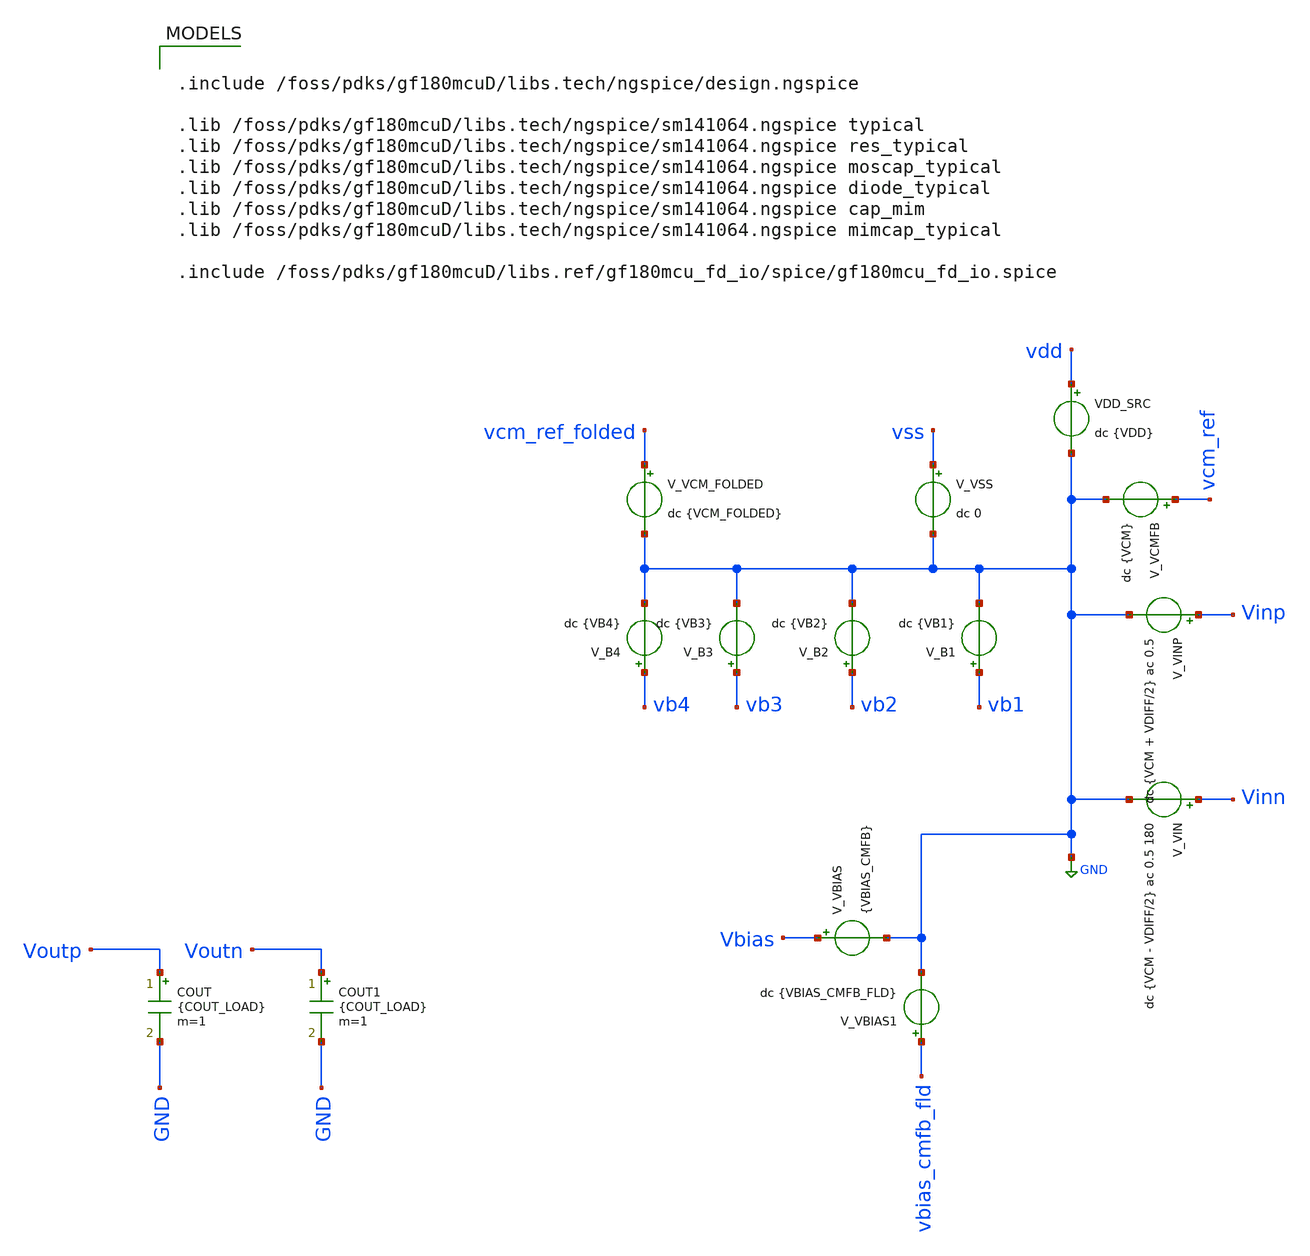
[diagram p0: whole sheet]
** sch_path: circuit_files/sar_adc_test/xschem/untitled.sch
**.subckt untitled
V_VIN Vinn GND dc {VCM - VDIFF/2} ac 0.5 180
VDD_SRC vdd GND dc {VDD}
V_VINP Vinp GND dc {VCM + VDIFF/2} ac 0.5
V_VSS vss GND dc 0
V_VCMFB vcm_ref GND dc {VCM}
V_B1 vb1 GND dc {VB1}
V_B2 vb2 GND dc {VB2}
V_B3 vb3 GND dc {VB3}
V_B4 vb4 GND dc {VB4}
V_VCM_FOLDED vcm_ref_folded GND dc {VCM_FOLDED}
V_VBIAS Vbias GND {VBIAS_CMFB}
V_VBIAS1 vbias_cmfb_fld GND dc {VBIAS_CMFB_FLD}
COUT Voutp GND {COUT_LOAD} m=1
COUT1 Voutn GND {COUT_LOAD} m=1
**** begin user architecture code

.include /foss/pdks/gf180mcuD/libs.tech/ngspice/design.ngspice

.lib /foss/pdks/gf180mcuD/libs.tech/ngspice/sm141064.ngspice typical
.lib /foss/pdks/gf180mcuD/libs.tech/ngspice/sm141064.ngspice res_typical
.lib /foss/pdks/gf180mcuD/libs.tech/ngspice/sm141064.ngspice moscap_typical
.lib /foss/pdks/gf180mcuD/libs.tech/ngspice/sm141064.ngspice diode_typical
.lib /foss/pdks/gf180mcuD/libs.tech/ngspice/sm141064.ngspice cap_mim
.lib /foss/pdks/gf180mcuD/libs.tech/ngspice/sm141064.ngspice mimcap_typical

.include /foss/pdks/gf180mcuD/libs.ref/gf180mcu_fd_io/spice/gf180mcu_fd_io.spice




**** begin user architecture code

.param sw_stat_mismatch=0
.param mis_vth=0
.param mis_k=0

.param VDD=3.3
.param VCM=1.65
.param VCM_FOLDED=1.60
.param VDIFF=0

* ============================================================
* Final selected OTA bias
* ============================================================
.param VB1=0.58
.param VB2=2.637
.param VB3=2.25
.param VB4=1.15

.param VBIAS_CMFB=0.82
.param VBIAS_CMFB_FLD=2.55

* ============================================================
* Compensation / load
* ============================================================
.param Cn=500f
.param Rn=8k
.param COUT_LOAD=200f

* Output CMFB sense resistors
.param Rcm=1Meg

* Folded-node CMFB sense resistors
.param Rcm_fld=20Meg

.param CCMFB=500f
.param CCMFB_FLD=1p

.options reltol=1e-4 abstol=1e-12 vntol=1e-6
.options gmin=1e-12
.options plotwinsize=0
.options method=gear maxord=2

* ============================================================
* Operating-point hints only. These do not force final OP.
* ============================================================
.nodeset V(voutp)=1.643
.nodeset V(voutn)=1.643
.nodeset V(vcm_sense)=1.643
.nodeset V(vbias_out)=0.866
.nodeset V(vx)=3.022
.nodeset V(vy)=3.022
.nodeset V(va)=2.401
.nodeset V(vb)=2.401
.nodeset V(net1)=0.887
.nodeset V(net4)=0.426
.nodeset V(net5)=0.426
.nodeset V(vcm_sense_folded)=1.600
.nodeset V(vb5)=0.713
.nodeset V(net8)=0.578
.nodeset V(net9)=2.624

.control

set noaskquit
set wr_singlescale
set appendwrite
set measdgt=8

shell rm -f ota_summary_report.txt
shell rm -f ota_detailed_report.txt
shell rm -f ota_ac_response.txt

echo ================================================== > ota_summary_report.txt
echo FINAL FULLY-DIFFERENTIAL OTA SUMMARY REPORT >> ota_summary_report.txt
echo PMOS-INPUT FOLDED-CMFB VERSION >> ota_summary_report.txt
echo ================================================== >> ota_summary_report.txt

echo ================================================== > ota_detailed_report.txt
echo FINAL FULLY-DIFFERENTIAL OTA DETAILED REPORT >> ota_detailed_report.txt
echo PMOS-INPUT FOLDED-CMFB VERSION >> ota_detailed_report.txt
echo ================================================== >> ota_detailed_report.txt

echo ---------------- PARAMETERS ---------------- >> ota_summary_report.txt
echo VDD=3.3 VCM=1.65 VDIFF=0 VCM_FOLDED=1.60 >> ota_summary_report.txt
echo VB1=0.58 VB2=2.637 VB3=2.25 VB4=1.15 >> ota_summary_report.txt
echo VBIAS_CMFB=0.82 VBIAS_CMFB_FLD=2.55 >> ota_summary_report.txt
echo Cn=500f Rn=8k COUT_LOAD=200f Rcm=1Meg Rcm_fld=20Meg CCMFB=500f CCMFB_FLD=1p >>
+ ota_summary_report.txt
echo -------------------------------------------------- >> ota_summary_report.txt

echo ---------------- PARAMETERS ---------------- >> ota_detailed_report.txt
echo VDD=3.3 VCM=1.65 VDIFF=0 >> ota_detailed_report.txt
echo VCM_FOLDED=1.60 >> ota_detailed_report.txt
echo VB1=0.58 VB2=2.637 VB3=2.25 VB4=1.15 >> ota_detailed_report.txt
echo VBIAS_CMFB=0.82 VBIAS_CMFB_FLD=2.55 >> ota_detailed_report.txt
echo Cn=500f Rn=8k COUT_LOAD=200f >> ota_detailed_report.txt
echo Rcm=1Meg Rcm_fld=20Meg CCMFB=500f CCMFB_FLD=1p >> ota_detailed_report.txt
echo -------------------------------------------------- >> ota_detailed_report.txt

* ============================================================
* DC OPERATING POINT
* ============================================================
op

* Numeric constants for ngspice control expressions.
* Do not use .param names directly inside let expressions.
let vdd_num         = 3.3
let vcm_num         = 1.65

let voutcm_op       = 0.5*(v(voutp)+v(voutn))
let voutdiff_op     = v(voutp)-v(voutn)
let va_cm_op        = 0.5*(v(va)+v(vb))
let vx_cm_op        = 0.5*(v(vx)+v(vy))
let net45_cm_op     = 0.5*(v(net4)+v(net5))

let idd_op          = -i(VDD_SRC)
let pdc_op          = vdd_num*idd_op

let folded_cm_err   = v(vcm_sense_folded)-v(vcm_ref_folded)
let out_cm_err      = voutcm_op-vcm_num

echo ---------------- OP SUMMARY ---------------- >> ota_summary_report.txt
echo VOUTP VOUTN VOUTCM VOUTDIFF OUT_CM_ERR >> ota_summary_report.txt
echo $&v(voutp) $&v(voutn) $&voutcm_op $&voutdiff_op $&out_cm_err >> ota_summary_report.txt
echo VA VB VA_CM VCM_SENSE_FOLDED VCM_REF_FOLDED FOLDED_CM_ERR >> ota_summary_report.txt
echo $&v(va) $&v(vb) $&va_cm_op $&v(vcm_sense_folded) $&v(vcm_ref_folded) $&folded_cm_err >>
+ ota_summary_report.txt
echo VBIAS_OUT VB5 NET8 NET9 IDD PDC >> ota_summary_report.txt
echo $&v(vbias_out) $&v(vb5) $&v(net8) $&v(net9) $&idd_op $&pdc_op >> ota_summary_report.txt
echo -------------------------------------------------- >> ota_summary_report.txt

echo ---------------- OP DETAILED NODES ---------------- >> ota_detailed_report.txt
echo VOUTP=$&v(voutp) >> ota_detailed_report.txt
echo VOUTN=$&v(voutn) >> ota_detailed_report.txt
echo VOUTCM=$&voutcm_op >> ota_detailed_report.txt
echo VOUTDIFF=$&voutdiff_op >> ota_detailed_report.txt
echo OUT_CM_ERR=$&out_cm_err >> ota_detailed_report.txt
echo VCM_SENSE_OUTPUT=$&v(vcm_sense) >> ota_detailed_report.txt
echo VBIAS_OUT=$&v(vbias_out) >> ota_detailed_report.txt
echo VX=$&v(vx) >> ota_detailed_report.txt
echo VY=$&v(vy) >> ota_detailed_report.txt
echo VX_CM=$&vx_cm_op >> ota_detailed_report.txt
echo VA=$&v(va) >> ota_detailed_report.txt
echo VB=$&v(vb) >> ota_detailed_report.txt
echo VA_CM=$&va_cm_op >> ota_detailed_report.txt
echo NET1=$&v(net1) >> ota_detailed_report.txt
echo NET4=$&v(net4) >> ota_detailed_report.txt
echo NET5=$&v(net5) >> ota_detailed_report.txt
echo NET4_NET5_CM=$&net45_cm_op >> ota_detailed_report.txt
echo VCM_REF_FOLDED=$&v(vcm_ref_folded) >> ota_detailed_report.txt
echo VCM_SENSE_FOLDED=$&v(vcm_sense_folded) >> ota_detailed_report.txt
echo FOLDED_CM_ERR=$&folded_cm_err >> ota_detailed_report.txt
echo VB5=$&v(vb5) >> ota_detailed_report.txt
echo NET8=$&v(net8) >> ota_detailed_report.txt
echo NET9=$&v(net9) >> ota_detailed_report.txt
echo IDD=$&idd_op >> ota_detailed_report.txt
echo PDC=$&pdc_op >> ota_detailed_report.txt
echo -------------------------------------------------- >> ota_detailed_report.txt

print v(voutp) v(voutn) voutcm_op voutdiff_op out_cm_err
print v(vcm_sense) v(vbias_out)
print v(vx) v(vy) vx_cm_op
print v(va) v(vb) va_cm_op
print v(net1) v(net4) v(net5) net45_cm_op
print v(vcm_ref_folded) v(vcm_sense_folded) folded_cm_err
print v(vb5) v(net8) v(net9)
print idd_op pdc_op

* ============================================================
* DIFFERENTIAL AC ANALYSIS
* Existing sources should be:
*   Vinp: dc {VCM + VDIFF/2} ac 0.5
*   Vinn: dc {VCM - VDIFF/2} ac 0.5 180
* This gives vin_diff = 1 V.
* ============================================================
ac dec 200 1 1G

let vin_diff       = v(vinp)-v(vinn)
let vin_cm         = 0.5*(v(vinp)+v(vinn))
let vin_diff_mag   = mag(vin_diff)
let vin_cm_mag     = mag(vin_cm)

let vout_diff      = v(voutp)-v(voutn)
let vout_cm_ac     = 0.5*(v(voutp)+v(voutn))

let avd            = vout_diff/vin_diff
let avd_mag        = mag(avd)
let avd_db         = 20*log10(avd_mag+1e-30)

* In this ngspice setup, cph() is returning radians.
let avd_phase_rad  = cph(avd)
let avd_phase_deg  = 57.2957795*avd_phase_rad

let gain_voutp     = v(voutp)/vin_diff
let gain_voutn     = v(voutn)/vin_diff
let gain_cmout     = vout_cm_ac/vin_diff

let gain_vxvy      = (v(vx)-v(vy))/vin_diff
let gain_vavb      = (v(va)-v(vb))/vin_diff
let gain_stage2    = avd/(gain_vavb+1e-30)

let gain_voutp_db  = 20*log10(mag(gain_voutp)+1e-30)
let gain_voutn_db  = 20*log10(mag(gain_voutn)+1e-30)
let gain_cmout_db  = 20*log10(mag(gain_cmout)+1e-30)

let gain_vxvy_db   = 20*log10(mag(gain_vxvy)+1e-30)
let gain_vavb_db   = 20*log10(mag(gain_vavb)+1e-30)
let gain_stage2_db = 20*log10(mag(gain_stage2)+1e-30)

let gain_vx_db     = 20*log10(mag(v(vx)/vin_diff)+1e-30)
let gain_vy_db     = 20*log10(mag(v(vy)/vin_diff)+1e-30)
let gain_va_db     = 20*log10(mag(v(va)/vin_diff)+1e-30)
let gain_vb_db     = 20*log10(mag(v(vb)/vin_diff)+1e-30)
let gain_net4_db   = 20*log10(mag(v(net4)/vin_diff)+1e-30)
let gain_net5_db   = 20*log10(mag(v(net5)/vin_diff)+1e-30)

* ============================================================
* 1 Hz low-frequency measurements
* ============================================================
meas ac VIN_DIFF_1HZ          find vin_diff_mag   at=1
meas ac VIN_CM_1HZ            find vin_cm_mag     at=1

meas ac AVD_MAG_1HZ           find avd_mag        at=1
meas ac AVD_DB_1HZ            find avd_db         at=1
meas ac AVD_PHASE_1HZ_RAD     find avd_phase_rad  at=1
meas ac AVD_PHASE_1HZ_DEG     find avd_phase_deg  at=1

meas ac GAIN_VOUTP_DB_1HZ     find gain_voutp_db  at=1
meas ac GAIN_VOUTN_DB_1HZ     find gain_voutn_db  at=1
meas ac GAIN_CMOUT_DB_1HZ     find gain_cmout_db  at=1

meas ac GAIN_VX_DB_1HZ        find gain_vx_db     at=1
meas ac GAIN_VY_DB_1HZ        find gain_vy_db     at=1
meas ac GAIN_VA_DB_1HZ        find gain_va_db     at=1
meas ac GAIN_VB_DB_1HZ        find gain_vb_db     at=1
meas ac GAIN_NET4_DB_1HZ      find gain_net4_db   at=1
meas ac GAIN_NET5_DB_1HZ      find gain_net5_db   at=1

meas ac GAIN_VXVY_DB_1HZ      find gain_vxvy_db   at=1
meas ac GAIN_VAVB_DB_1HZ      find gain_vavb_db   at=1
meas ac GAIN_STAGE2_DB_1HZ    find gain_stage2_db at=1

* ============================================================
* Dominant pole, UGF, and phase margin
* ============================================================
let avd_3db_target = avd_db_1hz - 3
meas ac FP_DOM when avd_db=avd_3db_target fall=1

meas ac UGF when avd_db=0 fall=1
meas ac PHASE_AT_UGF_RAD find avd_phase_rad when avd_db=0 fall=1
meas ac PHASE_AT_UGF_DEG find avd_phase_deg when avd_db=0 fall=1

let PM_EST = 180 + phase_at_ugf_deg

* ============================================================
* Useful spot checks
* ============================================================
meas ac AVD_DB_10K         find avd_db        at=10k
meas ac AVD_DB_100K        find avd_db        at=100k
meas ac AVD_DB_1MEG        find avd_db        at=1Meg
meas ac AVD_DB_10MEG       find avd_db        at=10Meg
meas ac AVD_DB_100MEG      find avd_db        at=100Meg

meas ac PHASE_10K_RAD      find avd_phase_rad at=10k
meas ac PHASE_100K_RAD     find avd_phase_rad at=100k
meas ac PHASE_1MEG_RAD     find avd_phase_rad at=1Meg
meas ac PHASE_10MEG_RAD    find avd_phase_rad at=10Meg
meas ac PHASE_100MEG_RAD   find avd_phase_rad at=100Meg

meas ac PHASE_10K_DEG      find avd_phase_deg at=10k
meas ac PHASE_100K_DEG     find avd_phase_deg at=100k
meas ac PHASE_1MEG_DEG     find avd_phase_deg at=1Meg
meas ac PHASE_10MEG_DEG    find avd_phase_deg at=10Meg
meas ac PHASE_100MEG_DEG   find avd_phase_deg at=100Meg

* ============================================================
* WRITE SUMMARY REPORT
* ============================================================
echo ---------------- AC SUMMARY ---------------- >> ota_summary_report.txt
echo VIN_DIFF_1HZ=$&vin_diff_1hz >> ota_summary_report.txt
echo VIN_CM_1HZ=$&vin_cm_1hz >> ota_summary_report.txt
echo DC_DIFF_GAIN_LINEAR=$&avd_mag_1hz >> ota_summary_report.txt
echo DC_DIFF_GAIN_DB=$&avd_db_1hz >> ota_summary_report.txt
echo DC_PHASE_1HZ_RAD=$&avd_phase_1hz_rad >> ota_summary_report.txt
echo DC_PHASE_1HZ_DEG=$&avd_phase_1hz_deg >> ota_summary_report.txt
echo STAGE1_GAIN_VAVB_DB=$&gain_vavb_db_1hz >> ota_summary_report.txt
echo STAGE2_GAIN_EST_DB=$&gain_stage2_db_1hz >> ota_summary_report.txt
echo DOMINANT_POLE_HZ=$&fp_dom >> ota_summary_report.txt
echo UNITY_GAIN_FREQ_HZ=$&ugf >> ota_summary_report.txt
echo PHASE_AT_UGF_RAD=$&phase_at_ugf_rad >> ota_summary_report.txt
echo PHASE_AT_UGF_DEG=$&phase_at_ugf_deg >> ota_summary_report.txt
echo PHASE_MARGIN_EST_DEG=$&PM_EST >> ota_summary_report.txt
echo -------------------------------------------------- >> ota_summary_report.txt

echo ---------------- PASS TARGETS TO CHECK ---------------- >> ota_summary_report.txt
echo Output CM target: VOUTCM should be near 1.65 V >> ota_summary_report.txt
echo Folded CMFB target: vcm_sense_folded should be near VCM_FOLDED >> ota_summary_report.txt
echo IDD target for this revision: roughly 100 uA to 300 uA is reasonable >> ota_summary_report.txt
echo Gain target: AVD should be greater than 70 dB before layout >> ota_summary_report.txt
echo Phase-margin target: PM_EST should be greater than 60 deg >> ota_summary_report.txt
echo Note: In this run cph is treated as radians and converted to degrees. >> ota_summary_report.txt
echo ================================================== >> ota_summary_report.txt

* ============================================================
* WRITE DETAILED REPORT
* ============================================================
echo ---------------- AC DETAILED LOW-FREQUENCY GAINS ---------------- >> ota_detailed_report.txt
echo VIN_DIFF_1HZ=$&vin_diff_1hz >> ota_detailed_report.txt
echo VIN_CM_1HZ=$&vin_cm_1hz >> ota_detailed_report.txt
echo AVD_MAG_1HZ=$&avd_mag_1hz >> ota_detailed_report.txt
echo AVD_DB_1HZ=$&avd_db_1hz >> ota_detailed_report.txt
echo AVD_PHASE_1HZ_RAD=$&avd_phase_1hz_rad >> ota_detailed_report.txt
echo AVD_PHASE_1HZ_DEG=$&avd_phase_1hz_deg >> ota_detailed_report.txt
echo GAIN_VOUTP_DB_1HZ=$&gain_voutp_db_1hz >> ota_detailed_report.txt
echo GAIN_VOUTN_DB_1HZ=$&gain_voutn_db_1hz >> ota_detailed_report.txt
echo GAIN_CMOUT_DB_1HZ=$&gain_cmout_db_1hz >> ota_detailed_report.txt
echo GAIN_VX_DB_1HZ=$&gain_vx_db_1hz >> ota_detailed_report.txt
echo GAIN_VY_DB_1HZ=$&gain_vy_db_1hz >> ota_detailed_report.txt
echo GAIN_VA_DB_1HZ=$&gain_va_db_1hz >> ota_detailed_report.txt
echo GAIN_VB_DB_1HZ=$&gain_vb_db_1hz >> ota_detailed_report.txt
echo GAIN_NET4_DB_1HZ=$&gain_net4_db_1hz >> ota_detailed_report.txt
echo GAIN_NET5_DB_1HZ=$&gain_net5_db_1hz >> ota_detailed_report.txt
echo GAIN_VXVY_DB_1HZ=$&gain_vxvy_db_1hz >> ota_detailed_report.txt
echo GAIN_VAVB_DB_1HZ=$&gain_vavb_db_1hz >> ota_detailed_report.txt
echo GAIN_STAGE2_DB_1HZ=$&gain_stage2_db_1hz >> ota_detailed_report.txt
echo -------------------------------------------------- >> ota_detailed_report.txt

echo ---------------- AC BANDWIDTH AND PHASE ---------------- >> ota_detailed_report.txt
echo AVD_3DB_TARGET=$&avd_3db_target >> ota_detailed_report.txt
echo FP_DOM_HZ=$&fp_dom >> ota_detailed_report.txt
echo UGF_HZ=$&ugf >> ota_detailed_report.txt
echo PHASE_AT_UGF_RAD=$&phase_at_ugf_rad >> ota_detailed_report.txt
echo PHASE_AT_UGF_DEG=$&phase_at_ugf_deg >> ota_detailed_report.txt
echo PHASE_MARGIN_EST_DEG=$&PM_EST >> ota_detailed_report.txt
echo AVD_DB_10K=$&avd_db_10k PHASE_10K_RAD=$&phase_10k_rad PHASE_10K_DEG=$&phase_10k_deg >>
+ ota_detailed_report.txt
echo AVD_DB_100K=$&avd_db_100k PHASE_100K_RAD=$&phase_100k_rad PHASE_100K_DEG=$&phase_100k_deg >>
+ ota_detailed_report.txt
echo AVD_DB_1MEG=$&avd_db_1meg PHASE_1MEG_RAD=$&phase_1meg_rad PHASE_1MEG_DEG=$&phase_1meg_deg >>
+ ota_detailed_report.txt
echo AVD_DB_10MEG=$&avd_db_10meg PHASE_10MEG_RAD=$&phase_10meg_rad PHASE_10MEG_DEG=$&phase_10meg_deg
+ >> ota_detailed_report.txt
echo AVD_DB_100MEG=$&avd_db_100meg PHASE_100MEG_RAD=$&phase_100meg_rad
+ PHASE_100MEG_DEG=$&phase_100meg_deg >> ota_detailed_report.txt
echo -------------------------------------------------- >> ota_detailed_report.txt

echo ---------------- INTERPRETATION NOTES ---------------- >> ota_detailed_report.txt
echo 1. If FOLDED_CM_ERR is near 0, the folded PMOS-CMFB is regulating. >> ota_detailed_report.txt
echo 2. If VBIAS_OUT is around 0.6 to 1.0 V, the output CMFB is in a reasonable range. >>
+ ota_detailed_report.txt
echo 3. If VA_CM is around 2.3 to 2.45 V, the second-stage PMOS gates are no longer over-driven. >>
+ ota_detailed_report.txt
echo 4. If IDD is around hundreds of uA, the previous mA shoot-through state is fixed. >>
+ ota_detailed_report.txt
echo 5. If STAGE1_GAIN_VAVB_DB is much greater than 30 dB, folded-node loading is no longer
+ dominating. >> ota_detailed_report.txt
echo 6. PM_EST is calculated using phase converted from radians to degrees. >>
+ ota_detailed_report.txt
echo 7. This is still pre-layout. Recheck after PEX and corners. >> ota_detailed_report.txt
echo ================================================== >> ota_detailed_report.txt

* ============================================================
* SAVE FULL AC TABLE
* Columns:
* frequency, avd_db, avd_phase_deg, gain_vavb_db,
* gain_stage2_db, gain_cmout_db, gain_voutp_db, gain_voutn_db
* ============================================================
wrdata ota_ac_response.txt avd_db avd_phase_deg gain_vavb_db gain_stage2_db gain_cmout_db
+ gain_voutp_db gain_voutn_db

* ============================================================
* PRINT IMPORTANT VALUES TO TERMINAL
* ============================================================
print avd_mag_1hz avd_db_1hz gain_vavb_db_1hz gain_stage2_db_1hz
print fp_dom ugf phase_at_ugf_rad phase_at_ugf_deg PM_EST
print avd_db_10k avd_db_100k avd_db_1meg avd_db_10meg avd_db_100meg
print phase_10k_deg phase_100k_deg phase_1meg_deg phase_10meg_deg phase_100meg_deg

echo ==================================================
echo Done.
echo Generated:
echo   ota_summary_report.txt
echo   ota_detailed_report.txt
echo   ota_ac_response.txt
echo ==================================================

.endc

**** end user architecture code



**** end user architecture code
**.ends
.GLOBAL GND
.end
